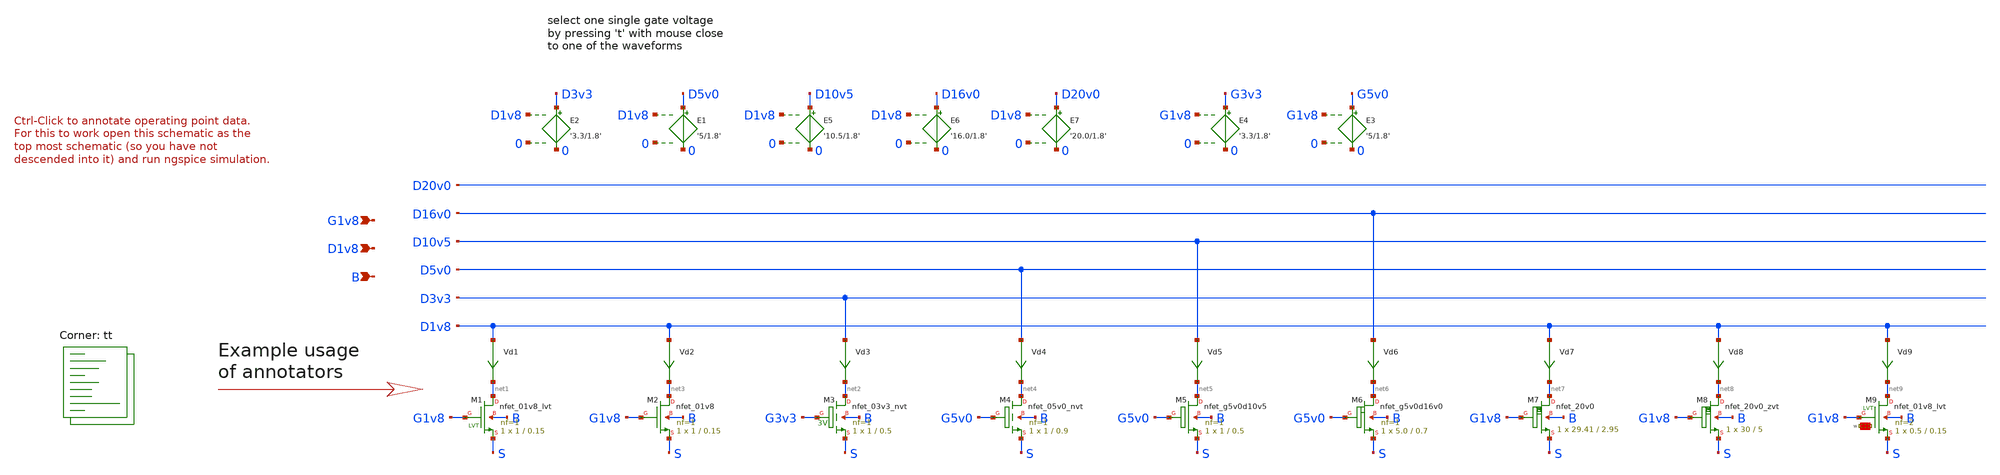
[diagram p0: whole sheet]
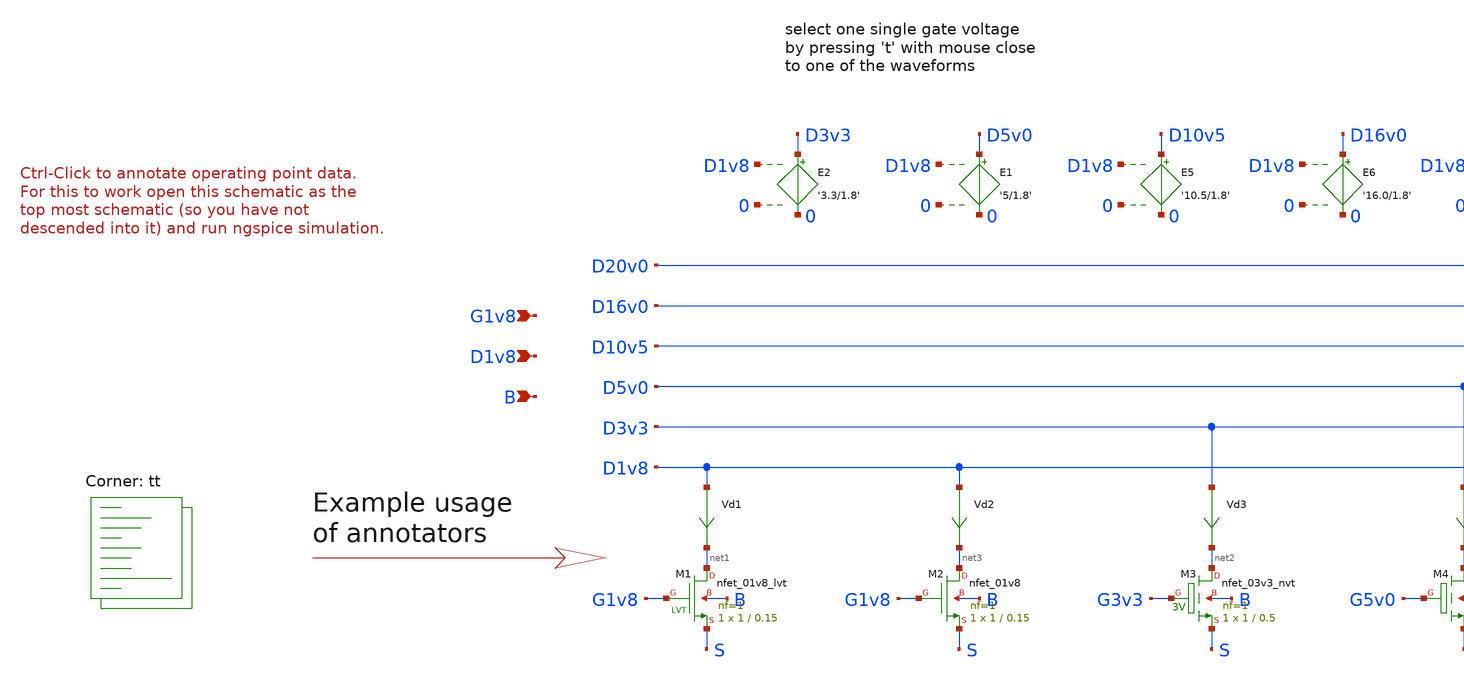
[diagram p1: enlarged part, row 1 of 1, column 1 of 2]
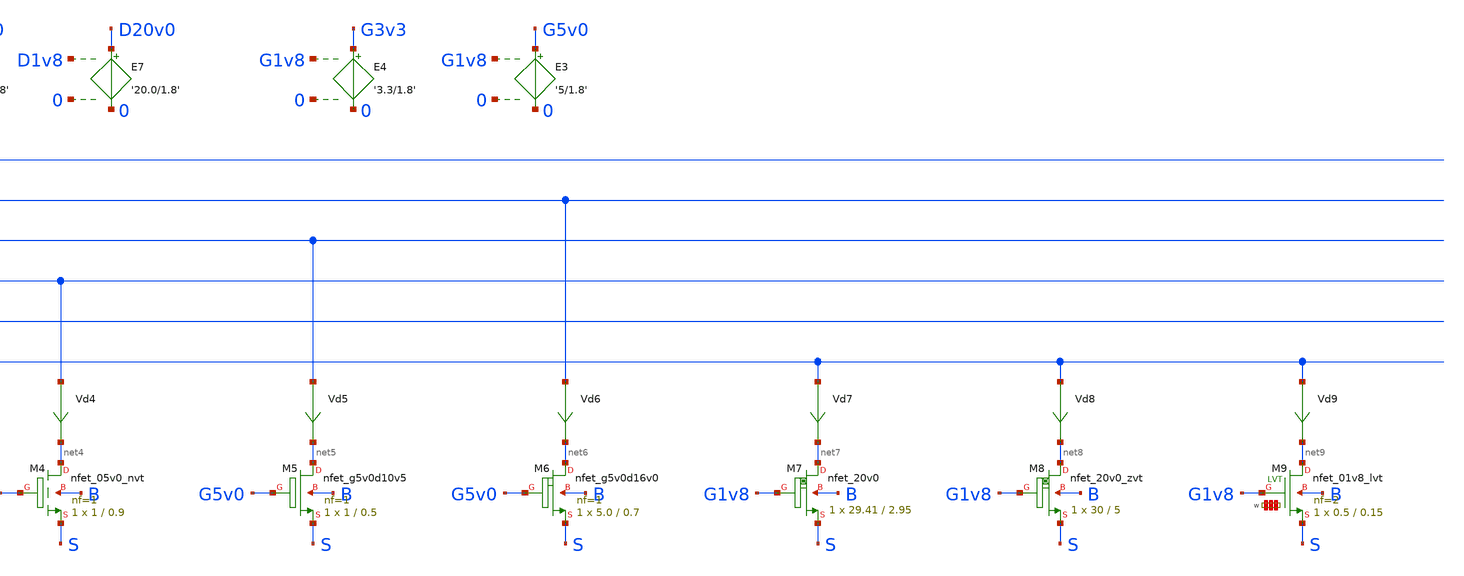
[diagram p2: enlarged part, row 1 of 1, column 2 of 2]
** sch_path: inverter1.sch
* Copyright 2021 Stefan Frederik Schippers
* Licensed under the Apache License, Version 2.0 (the "License");
* you may not use this file except in compliance with the License.
* You may obtain a copy of the License at
* https://www.apache.org/licenses/LICENSE-2.0
* Unless required by applicable law or agreed to in writing, software
* distributed under the License is distributed on an "AS IS" BASIS,
* WITHOUT WARRANTIES OR CONDITIONS OF ANY KIND, either express or implied.
* See the License for the specific language governing permissions and
* limitations under the License.
**.subckt inverter1 G1v8 D1v8 B
*.ipin G1v8
*.ipin D1v8
*.ipin B
Vd1 D1v8 net1 0
.save i(vd1)
Vd3 D3v3 net2 0
.save i(vd3)
Vd2 D1v8 net3 0
.save i(vd2)
Vd4 D5v0 net4 0
.save i(vd4)
E1 D5v0 0 D1v8 0 '5/1.8'
E2 D3v3 0 D1v8 0 '3.3/1.8'
E3 G5v0 0 G1v8 0 '5/1.8'
E4 G3v3 0 G1v8 0 '3.3/1.8'
Vd5 D10v5 net5 0
.save i(vd5)
E5 D10v5 0 D1v8 0 '10.5/1.8'
E6 D16v0 0 D1v8 0 '16.0/1.8'
Vd6 D16v0 net6 0
.save i(vd6)
Vd7 D1v8 net7 0
.save i(vd7)
E7 D20v0 0 D1v8 0 '20.0/1.8'
XM1 net1 G1v8 S B sky130_fd_pr__nfet_01v8_lvt L=0.15 W=1 nf=1 ad='int((1 + 1)/2) * 1 / 1 * 0.29' as='int((1 + 2)/2) * 1 / 1 * 0.29'
+ pd='2*int((1 + 1)/2) * (1 / 1 + 0.29)' ps='2*int((1 + 2)/2) * (1 / 1 + 0.29)' nrd='0.29 / 1 ' nrs='0.29 / 1 '
+ sa=0 sb=0 sd=0 mult=1 m=1
XM2 net3 G1v8 S B sky130_fd_pr__nfet_01v8 L=0.15 W=1 nf=1 ad='int((1 + 1)/2) * 1 / 1 * 0.29' as='int((1 + 2)/2) * 1 / 1 * 0.29'
+ pd='2*int((1 + 1)/2) * (1 / 1 + 0.29)' ps='2*int((1 + 2)/2) * (1 / 1 + 0.29)' nrd='0.29 / 1 ' nrs='0.29 / 1 '
+ sa=0 sb=0 sd=0 mult=1 m=1
XM3 net2 G3v3 S B sky130_fd_pr__nfet_03v3_nvt L=0.5 W=1 nf=1 ad='int((1 + 1)/2) * 1 / 1 * 0.29' as='int((1 + 2)/2) * 1 / 1 * 0.29'
+ pd='2*int((1 + 1)/2) * (1 / 1 + 0.29)' ps='2*int((1 + 2)/2) * (1 / 1 + 0.29)' nrd='0.29 / 1 ' nrs='0.29 / 1 '
+ sa=0 sb=0 sd=0 mult=1 m=1
XM4 net4 G5v0 S B sky130_fd_pr__nfet_05v0_nvt L=0.9 W=1 nf=1 ad='int((1 + 1)/2) * 1 / 1 * 0.29' as='int((1 + 2)/2) * 1 / 1 * 0.29'
+ pd='2*int((1 + 1)/2) * (1 / 1 + 0.29)' ps='2*int((1 + 2)/2) * (1 / 1 + 0.29)' nrd='0.29 / 1 ' nrs='0.29 / 1 '
+ sa=0 sb=0 sd=0 mult=1 m=1
XM5 net5 G5v0 S B sky130_fd_pr__nfet_g5v0d10v5 L=0.5 W=1 nf=1 ad='int((1 + 1)/2) * 1 / 1 * 0.29' as='int((1 + 2)/2) * 1 / 1 * 0.29'
+ pd='2*int((1 + 1)/2) * (1 / 1 + 0.29)' ps='2*int((1 + 2)/2) * (1 / 1 + 0.29)' nrd='0.29 / 1 ' nrs='0.29 / 1 '
+ sa=0 sb=0 sd=0 mult=1 m=1
XM6 net6 G5v0 S B sky130_fd_pr__nfet_g5v0d16v0 L=0.7 W=5.0 nf=1 ad='int((nf+1)/2) * W/nf * 0.29' as='int((nf+2)/2) * W/nf * 0.29'
+ pd='2*int((nf+1)/2) * (W/nf + 0.29)' ps='2*int((nf+2)/2) * (W/nf + 0.29)' nrd='0.29 / W' nrs='0.29 / W'
+ sa=0 sb=0 sd=0 mult=1 m=1
Vd8 D1v8 net8 0
.save i(vd8)
XM7 net7 G1v8 S B sky130_fd_pr__nfet_20v0 L=2.95 W=29.41 m=1
XM8 net8 G1v8 S B sky130_fd_pr__nfet_20v0_zvt W=30 L=5 m=1
Vd9 D1v8 net9 0
.save i(vd9)
XM9 net9 G1v8 S B sky130_fd_pr__nfet_01v8_lvt L=0.15 W='0.5 * 2 ' nf=2 ad='int((2 + 1)/2) * 0.5 / 2 * 0.29'
+ as='int((2 + 2)/2) * 0.5 / 2 * 0.29' pd='2*int((2 + 1)/2) * (0.5 / 2 + 0.29)' ps='2*int((2 + 2)/2) * (0.5 / 2 + 0.29)'
+ nrd='0.29 / 0.5 ' nrs='0.29 / 0.5 ' sa=0 sb=0 sd=0 mult=1 m=1
**** begin user architecture code

* this option enables mos model bin
* selection based on W/NF instead of W
.option wnflag=1
.option savecurrents
vg G1v8 0 1.8
vs s 0 0
vd D1v8 0 1.8
vb b 0 0
.control
save all
save @m.xm9.msky130_fd_pr__nfet_01v8_lvt[gm]
save @m.xm8.m1[gm]
save @m.xm7.m1[gm]
save @m.xm6.xmain1.msky130_fd_pr__nfet_g5v0d16v0__base[gm]
save @m.xm5.msky130_fd_pr__nfet_g5v0d10v5[gm]
save @m.xm4.msky130_fd_pr__nfet_05v0_nvt[gm]
save @m.xm3.msky130_fd_pr__nfet_03v3_nvt[gm]
save @m.xm2.msky130_fd_pr__nfet_01v8[gm]
save @m.xm1.msky130_fd_pr__nfet_01v8_lvt[gm]

dc vd 0 1.8 0.005 vg 0 1.8 0.2
write test_nmos.raw
* dc vd 0 1.8 0.001 vg 0 1.2 0.1
plot all.vd1#branch vs D1v8
*plot all.vd2#branch vs D1v8
plot all.vd3#branch vs D3v3
*plot all.vd4#branch vs D5v0
plot all.vd5#branch vs D10v5
*plot all.vd6#branch vs D16v0
plot all.vd8#branch vs D1v8
plot all.vd7#branch vs D1v8
set appendwrite
op
write test_nmos.raw
.endc


.lib $::SKYWATER_MODELS/sky130.lib.spice tt
**** end user architecture code
**.ends
.end
